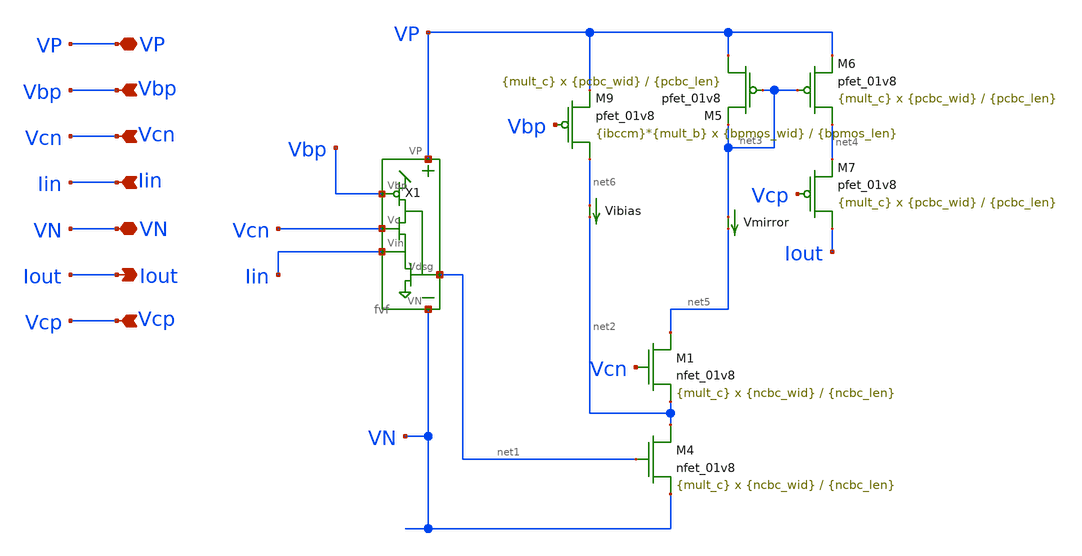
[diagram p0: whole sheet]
** sch_path: fvfccm.sch
**.subckt fvfccm Vbp Vcn Iin VP VN Iout Vcp
*.ipin Vbp
*.ipin Vcn
*.ipin Iin
*.iopin VP
*.iopin VN
*.opin Iout
*.ipin Vcp
XM4 net2 net1 VN VN sky130_fd_pr__nfet_01v8 L={ncbc_len} W={ncbc_wid} nf=1 ad='int((nf+1)/2) * W/nf * 0.29'
+ as='int((nf+2)/2) * W/nf * 0.29' pd='2*int((nf+1)/2) * (W/nf + 0.29)' ps='2*int((nf+2)/2) * (W/nf + 0.29)'
+ nrd='0.29 / W' nrs='0.29 / W' sa=0 sb=0 sd=0 mult={mult_c} m={mult_c}
XM5 VP net3 net3 VP sky130_fd_pr__pfet_01v8 L={pcbc_len} W={pcbc_wid} nf=1 ad='int((nf+1)/2) * W/nf * 0.29'
+ as='int((nf+2)/2) * W/nf * 0.29' pd='2*int((nf+1)/2) * (W/nf + 0.29)' ps='2*int((nf+2)/2) * (W/nf + 0.29)'
+ nrd='0.29 / W' nrs='0.29 / W' sa=0 sb=0 sd=0 mult={mult_c} m={mult_c}
XM6 net4 net3 VP VP sky130_fd_pr__pfet_01v8 L={pcbc_len} W={pcbc_wid} nf=1 ad='int((nf+1)/2) * W/nf * 0.29'
+ as='int((nf+2)/2) * W/nf * 0.29' pd='2*int((nf+1)/2) * (W/nf + 0.29)' ps='2*int((nf+2)/2) * (W/nf + 0.29)'
+ nrd='0.29 / W' nrs='0.29 / W' sa=0 sb=0 sd=0 mult={mult_c} m={mult_c}
XM7 Iout Vcp net4 VP sky130_fd_pr__pfet_01v8 L={pcbc_len} W={pcbc_wid} nf=1 ad='int((nf+1)/2) * W/nf * 0.29'
+ as='int((nf+2)/2) * W/nf * 0.29' pd='2*int((nf+1)/2) * (W/nf + 0.29)' ps='2*int((nf+2)/2) * (W/nf + 0.29)'
+ nrd='0.29 / W' nrs='0.29 / W' sa=0 sb=0 sd=0 mult={mult_c} m={mult_c}
XM9 net6 Vbp VP VP sky130_fd_pr__pfet_01v8 L={bpmos_len} W={bpmos_wid} nf=1 ad='int((nf+1)/2) * W/nf * 0.29'
+ as='int((nf+2)/2) * W/nf * 0.29' pd='2*int((nf+1)/2) * (W/nf + 0.29)' ps='2*int((nf+2)/2) * (W/nf + 0.29)'
+ nrd='0.29 / W' nrs='0.29 / W' sa=0 sb=0 sd=0 mult={ibccm}*{mult_b} m={ibccm}*{mult_b}
X1 VP Vbp Vcn Iin net1 VN fvf
Vmirror net3 net5 0
.save i(vmirror)
Vibias net6 net2 0
.save i(vibias)
XM1 net5 Vcn net2 VN sky130_fd_pr__nfet_01v8 L={ncbc_len} W={ncbc_wid} nf=1 ad='int((nf+1)/2) * W/nf * 0.29'
+ as='int((nf+2)/2) * W/nf * 0.29' pd='2*int((nf+1)/2) * (W/nf + 0.29)' ps='2*int((nf+2)/2) * (W/nf + 0.29)'
+ nrd='0.29 / W' nrs='0.29 / W' sa=0 sb=0 sd=0 mult={mult_c} m={mult_c}
**.ends

* expanding   symbol:  fvf.sym # of pins=6
** sym_path: fvf.sym
** sch_path: fvf.sch
.subckt fvf VP Vbp Vc Vin Vdsg VN
*.iopin VP
*.iopin VN
*.ipin Vbp
*.ipin Vc
*.ipin Vin
*.opin Vdsg
XM1 VP Vbp Vdsg GND sky130_fd_pr__nfet_01v8 L=0.15 W=1 nf=1 ad='int((nf+1)/2) * W/nf * 0.29' as='int((nf+2)/2) * W/nf * 0.29'
+ pd='2*int((nf+1)/2) * (W/nf + 0.29)' ps='2*int((nf+2)/2) * (W/nf + 0.29)' nrd='0.29 / W' nrs='0.29 / W'
+ sa=0 sb=0 sd=0 mult=1 m=1
XM2 Vdsg Vc Vin GND sky130_fd_pr__nfet_01v8 L=0.15 W=1 nf=1 ad='int((nf+1)/2) * W/nf * 0.29' as='int((nf+2)/2) * W/nf * 0.29'
+ pd='2*int((nf+1)/2) * (W/nf + 0.29)' ps='2*int((nf+2)/2) * (W/nf + 0.29)' nrd='0.29 / W' nrs='0.29 / W'
+ sa=0 sb=0 sd=0 mult=1 m=1
XM3 Vdsg Vc Vin GND sky130_fd_pr__nfet_01v8 L=0.15 W=1 nf=1 ad='int((nf+1)/2) * W/nf * 0.29' as='int((nf+2)/2) * W/nf * 0.29'
+ pd='2*int((nf+1)/2) * (W/nf + 0.29)' ps='2*int((nf+2)/2) * (W/nf + 0.29)' nrd='0.29 / W' nrs='0.29 / W'
+ sa=0 sb=0 sd=0 mult=1 m=1
XM4 VN Vdsg Vin GND sky130_fd_pr__nfet_01v8 L=0.15 W=1 nf=1 ad='int((nf+1)/2) * W/nf * 0.29' as='int((nf+2)/2) * W/nf * 0.29'
+ pd='2*int((nf+1)/2) * (W/nf + 0.29)' ps='2*int((nf+2)/2) * (W/nf + 0.29)' nrd='0.29 / W' nrs='0.29 / W'
+ sa=0 sb=0 sd=0 mult=1 m=1
.ends

.end
